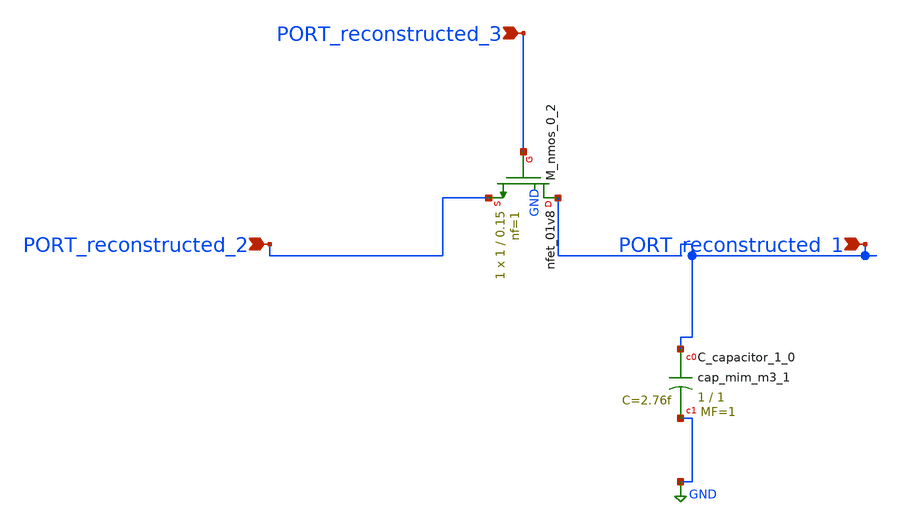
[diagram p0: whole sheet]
** sch_path: schematics/AMSNet/775.sch
**.subckt 775 PORT_reconstructed_3 PORT_reconstructed_2 PORT_reconstructed_1
*.ipin PORT_reconstructed_3
*.ipin PORT_reconstructed_2
*.ipin PORT_reconstructed_1
XC_capacitor_1_0 PORT_reconstructed_1 GND sky130_fd_pr__cap_mim_m3_1 W=1 L=1 MF=1 m=1
XM_nmos_0_2 PORT_reconstructed_1 PORT_reconstructed_3 PORT_reconstructed_2 GND sky130_fd_pr__nfet_01v8
+ L=0.15 W=1 nf=1 ad='int((1 + 1)/2) * 1 / 1 * 0.29' as='int((1 + 2)/2) * 1 / 1 * 0.29' pd='2*int((1 + 1)/2) * (1 / 1 + 0.29)'
+ ps='2*int((1 + 2)/2) * (1 / 1 + 0.29)' nrd='0.29 / 1 ' nrs='0.29 / 1 ' sa=0 sb=0 sd=0 mult=1 m=1
**.ends
.GLOBAL GND
.end
